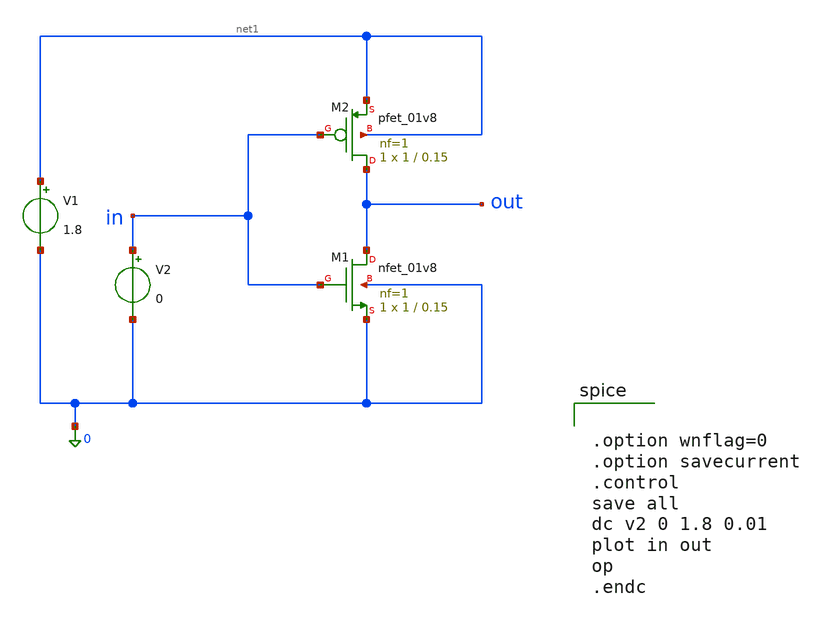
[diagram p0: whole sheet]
** sch_path: dsrt2026_Verdian.sch
**.subckt dsrt2026_Verdian
XM1 out in 0 0 sky130_fd_pr__nfet_01v8 L=0.15 W=1 nf=1 ad='int((1 + 1)/2) * 1 / 1 * 0.29' as='int((1 + 2)/2) * 1 / 1 * 0.29'
+ pd='2*int((1 + 1)/2) * (1 / 1 + 0.29)' ps='2*int((1 + 2)/2) * (1 / 1 + 0.29)' nrd='0.29 / 1 ' nrs='0.29 / 1 '
+ sa=0 sb=0 sd=0 mult=1 m=1
XM2 out in net1 net1 sky130_fd_pr__pfet_01v8 L=0.15 W=1 nf=1 ad='int((1 + 1)/2) * 1 / 1 * 0.29' as='int((1 + 2)/2) * 1 / 1 * 0.29'
+ pd='2*int((1 + 1)/2) * (1 / 1 + 0.29)' ps='2*int((1 + 2)/2) * (1 / 1 + 0.29)' nrd='0.29 / 1 ' nrs='0.29 / 1 '
+ sa=0 sb=0 sd=0 mult=1 m=1
V2 in 0 0
V1 net1 0 1.8
**** begin user architecture code
 .lib /foss/pdks/sky130A/libs.tech/ngspice/sky130.lib.spice tt

.param mc_mm_switch=0
.param mc_pr_switch=1



.option wnflag=0
.option savecurrent
.control
save all
dc v2 0 1.8 0.01
plot in out
op
.endc


**** end user architecture code
**.ends
.end
